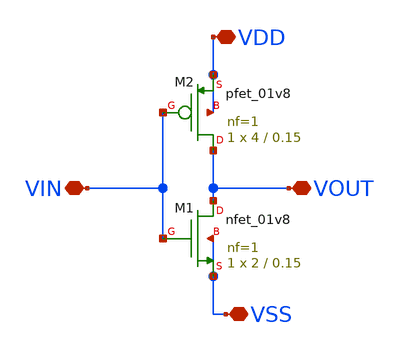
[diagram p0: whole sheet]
** sch_path: xschem/DC_DC_Converter_xschem/OTHERS/DC_DC_Converter_JV10/Delay_block_revised/inverter.sch
**.subckt inverter VDD VOUT VSS VIN
*.iopin VDD
*.iopin VOUT
*.iopin VSS
*.iopin VIN
XM1 VOUT VIN VSS VSS sky130_fd_pr__nfet_01v8 L=0.15 W=2 nf=1 ad='int((nf+1)/2) * W/nf * 0.29' as='int((nf+2)/2) * W/nf * 0.29'
+ pd='2*int((nf+1)/2) * (W/nf + 0.29)' ps='2*int((nf+2)/2) * (W/nf + 0.29)' nrd='0.29 / W' nrs='0.29 / W'
+ sa=0 sb=0 sd=0 mult=1 m=1
XM2 VOUT VIN VDD VDD sky130_fd_pr__pfet_01v8 L=0.15 W=4 nf=1 ad='int((nf+1)/2) * W/nf * 0.29' as='int((nf+2)/2) * W/nf * 0.29'
+ pd='2*int((nf+1)/2) * (W/nf + 0.29)' ps='2*int((nf+2)/2) * (W/nf + 0.29)' nrd='0.29 / W' nrs='0.29 / W'
+ sa=0 sb=0 sd=0 mult=1 m=1
**.ends
.end
